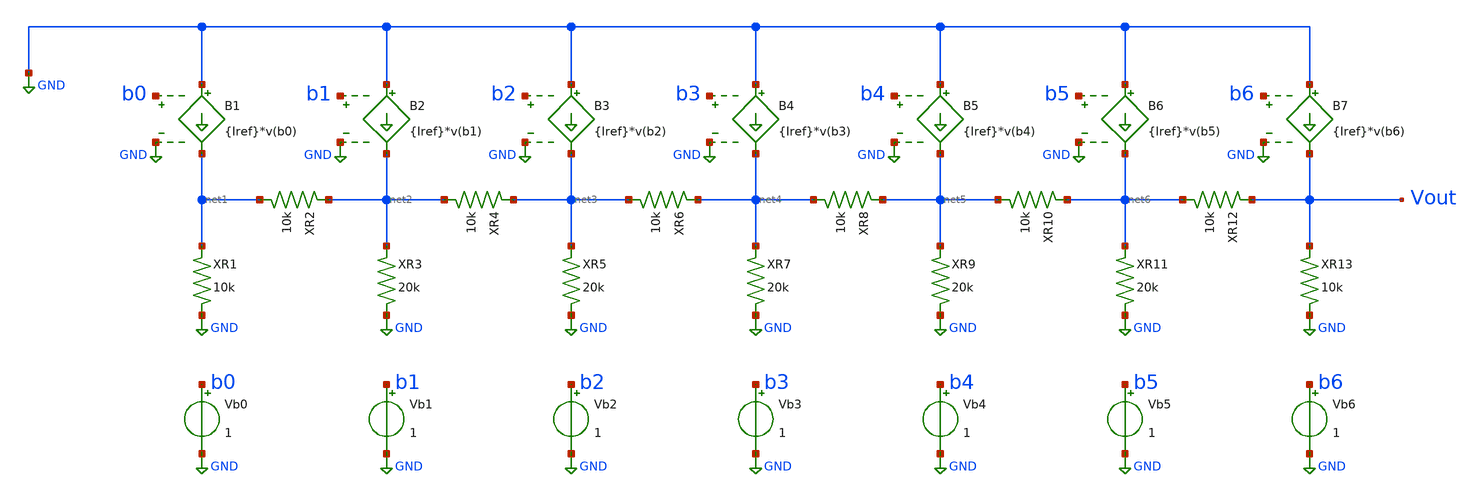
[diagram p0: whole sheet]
** sch_path: projects/montecarlo/xschem_ngspice/dactut/mcdactut/mcdactut.sch
**.subckt mcdactut
B1 GND net1 b0 GND {Iref}*v(b0)
XR1 net1 GND gaussres nom=10k
Vb0 b0 GND 1
XR2 net2 net1 gaussres nom=10k
B2 GND net2 b1 GND {Iref}*v(b1)
XR3 net2 GND gaussres nom=20k
Vb1 b1 GND 1
XR4 net3 net2 gaussres nom=10k
B3 GND net3 b2 GND {Iref}*v(b2)
XR5 net3 GND gaussres nom=20k
Vb2 b2 GND 1
XR6 net4 net3 gaussres nom=10k
B4 GND net4 b3 GND {Iref}*v(b3)
XR7 net4 GND gaussres nom=20k
Vb3 b3 GND 1
XR8 net5 net4 gaussres nom=10k
B5 GND net5 b4 GND {Iref}*v(b4)
XR9 net5 GND gaussres nom=20k
Vb4 b4 GND 1
XR10 net6 net5 gaussres nom=10k
B6 GND net6 b5 GND {Iref}*v(b5)
XR11 net6 GND gaussres nom=20k
Vb5 b5 GND 1
XR12 Vout net6 gaussres nom=10k
B7 GND Vout b6 GND {Iref}*v(b6)
XR13 Vout GND gaussres nom=10k
Vb6 b6 GND 1
**** begin user architecture code



.param MC_SWITCH=1.0

.subckt gaussres pos neg
.param nom=1k cv=0.005
R1 pos neg {nom + MC_SWITCH*AGAUSS(0,1,1)*cv*nom}
.ends

.option wnflag=1

.param Iref=100u

.control
  set wr_singlescale
  let runs = 10
  let run = 1
  while run <= runs
    set appendwrite = FALSE
    set wr_vecnames
    let code = 0
    while code < 128
      if code eq 0
        let b0 = 0
      else
        let b0 = code % 2
      end

      if floor(code / 2) eq 0
        let b1 = 0
      else
        let b1 = floor(code / 2) % 2
      end

      if floor(code / 4) eq 0
        let b2 = 0
      else
        let b2 = floor(code / 4) % 2
      end

      if floor(code / 8) eq 0
        let b3 = 0
      else
        let b3 = floor(code / 8) % 2
      end

      if floor(code / 16) eq 0
        let b4 = 0
      else
        let b4 = floor(code / 16) % 2
      end

      if floor(code / 32) eq 0
        let b5 = 0
      else
        let b5 = floor(code / 32) % 2
      end

      if floor(code / 64) eq 0
        let b6 = 0
      else
        let b6 = floor(code / 64) % 2
      end

      alter vb0 $&b0
      alter vb1 $&b1
      alter vb2 $&b2
      alter vb3 $&b3
      alter vb4 $&b4
      alter vb5 $&b5
      alter vb6 $&b6
      save all
      op
      wrdata /foss/designs/my_design/projects/montecarlo/xschem_ngspice/dactut/mcdactut/mcdactut{$&run}.txt
+ v(b0) v(b1) v(b2) v(b3) v(b4) v(b5) v(b6) v(Vout)/1e4 v(Vout)
      if code eq 0
        set appendwrite
        set wr_vecnames = FALSE
      end
      let code = code + 1
    end
    reset
    let run = run + 1
  end
  * quit
.endc






**** end user architecture code
**.ends
.GLOBAL GND
.end
